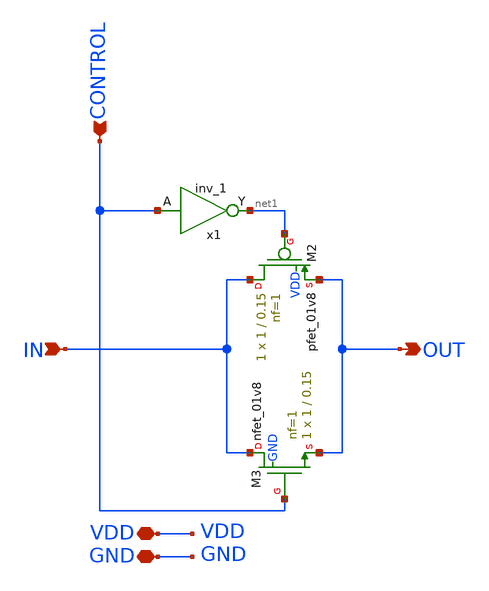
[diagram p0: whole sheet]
** sch_path: src/analog_source_files/transmition_gate.sch
**.subckt transmition_gate IN CONTROL OUT VDD GND
*.ipin IN
*.ipin CONTROL
*.opin OUT
*.iopin VDD
*.iopin GND
XM2 IN net1 OUT VDD sky130_fd_pr__pfet_01v8 L=0.15 W=1 nf=1 ad='int((1 + 1)/2) * 1 / 1 * 0.29' as='int((1 + 2)/2) * 1 / 1 * 0.29'
+ pd='2*int((1 + 1)/2) * (1 / 1 + 0.29)' ps='2*int((1 + 2)/2) * (1 / 1 + 0.29)' nrd='0.29 / 1 ' nrs='0.29 / 1 '
+ sa=0 sb=0 sd=0 mult=1 m=1
x1 CONTROL GND GND VDD VDD net1 sky130_fd_sc_hd__inv_1
XM3 IN CONTROL OUT GND sky130_fd_pr__nfet_01v8 L=0.15 W=1 nf=1 ad='int((1 + 1)/2) * 1 / 1 * 0.29' as='int((1 + 2)/2) * 1 / 1 * 0.29'
+ pd='2*int((1 + 1)/2) * (1 / 1 + 0.29)' ps='2*int((1 + 2)/2) * (1 / 1 + 0.29)' nrd='0.29 / 1 ' nrs='0.29 / 1 '
+ sa=0 sb=0 sd=0 mult=1 m=1
**.ends
.end
